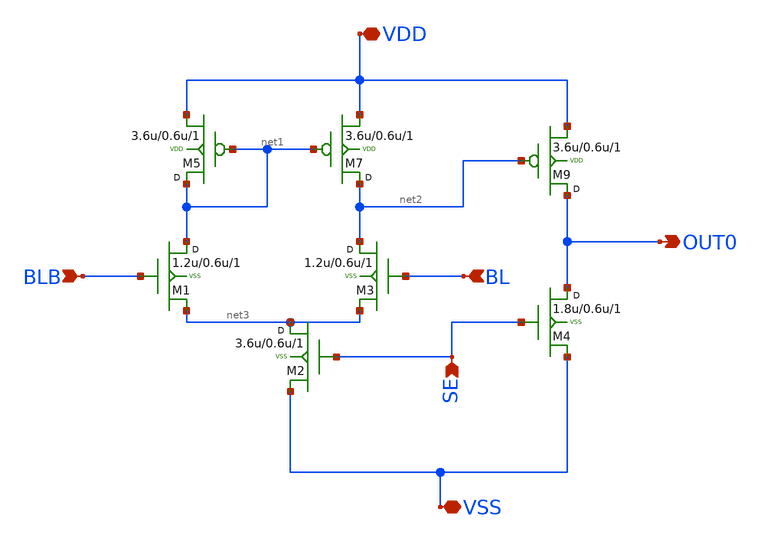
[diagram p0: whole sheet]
** sch_path: SRAM/senseamp/schematic/Senseamp.sch
**.subckt Senseamp BLB BL SE OUT0 VSS VDD
*.ipin BLB
*.ipin BL
*.ipin SE
*.opin OUT0
*.iopin VSS
*.iopin VDD
M7 net2 net1 VDD VDD pfet w=3.6u l=0.6u m=1
M9 OUT0 net2 VDD VDD pfet w=3.6u l=0.6u m=1
M1 net1 BLB net3 VSS nfet w=1.2u l=0.6u m=1
M2 net3 SE VSS VSS nfet w=3.6u l=0.6u m=1
M3 net2 BL net3 VSS nfet w=1.2u l=0.6u m=1
M4 OUT0 SE VSS VSS nfet w=1.8u l=0.6u m=1
M5 net1 net1 VDD VDD pfet w=3.6u l=0.6u m=1
**.ends
.end
